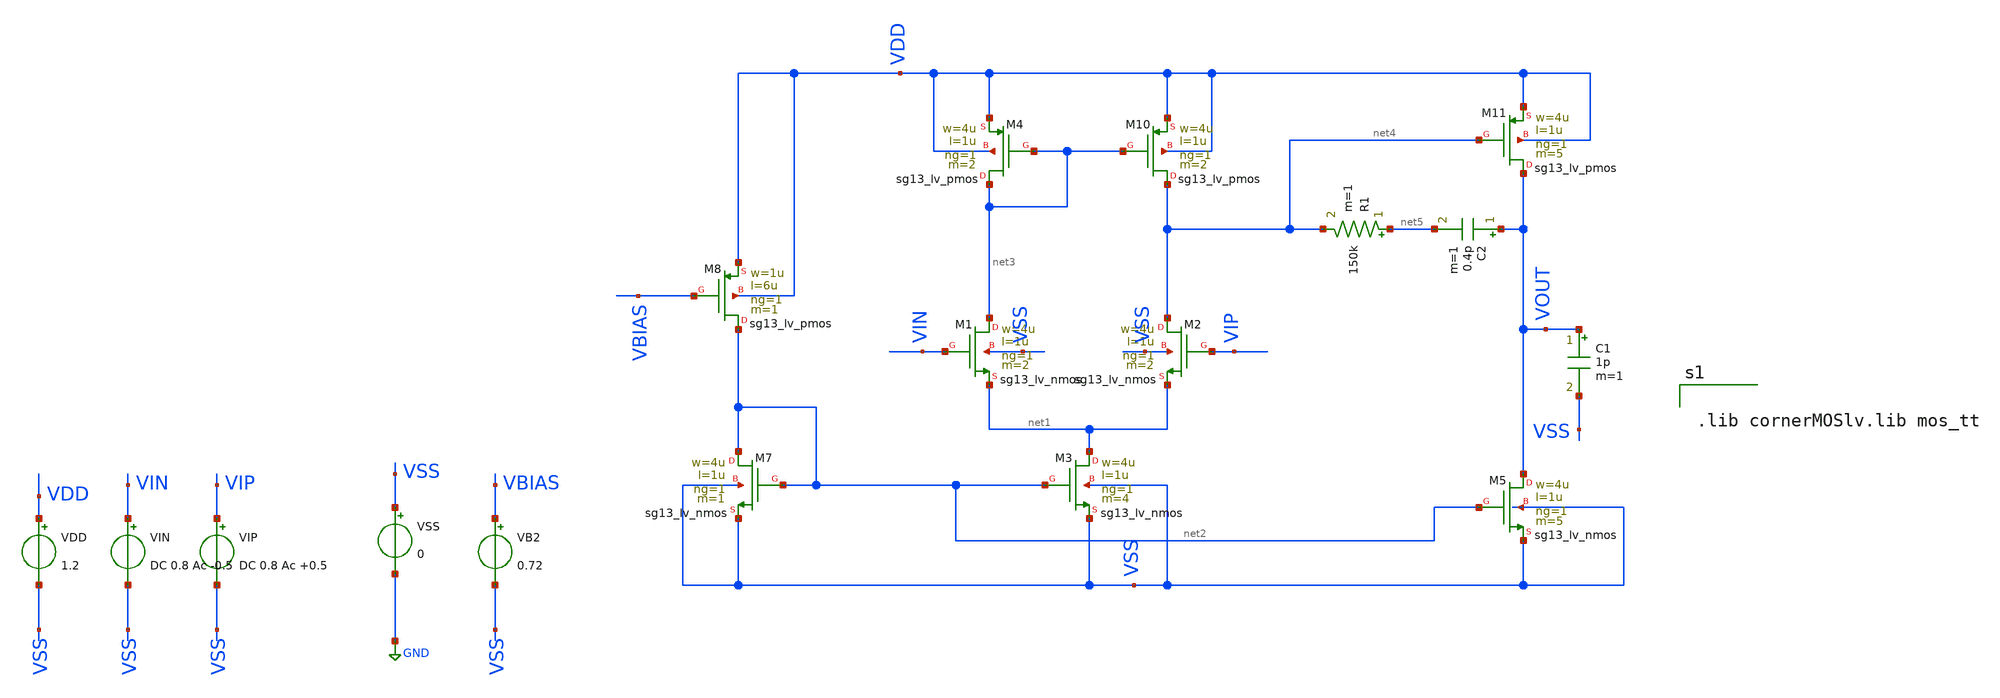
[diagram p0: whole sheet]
** sch_path: BTDay5-Ex/Ex1_6_Lecture5.sch
**.subckt Ex1_6_Lecture5
XM1 net3 VIN net1 VSS sg13_lv_nmos w=4u l=1u ng=1 m=2 mm_ok=1
XM2 net4 VIP net1 VSS sg13_lv_nmos w=4u l=1u ng=1 m=2 mm_ok=1
XM3 net1 net2 VSS VSS sg13_lv_nmos w=4u l=1u ng=1 m=4 mm_ok=1
VDD VDD VSS 1.2
VIN VIN VSS DC 0.8 Ac -0.5
VIP VIP VSS DC 0.8 Ac +0.5
VSS VSS GND 0
XM4 net3 net3 VDD VDD sg13_lv_pmos w=4u l=1u ng=1 m=2 mm_ok=1
XM7 net2 net2 VSS VSS sg13_lv_nmos w=4u l=1u ng=1 m=1 mm_ok=1
XM8 net2 VBIAS VDD VDD sg13_lv_pmos w=1u l=6u ng=1 m=1 mm_ok=1
XM10 net4 net3 VDD VDD sg13_lv_pmos w=4u l=1u ng=1 m=2 mm_ok=1
VB2 VBIAS VSS 0.72
XM5 VOUT net2 VSS VSS sg13_lv_nmos w=4u l=1u ng=1 m=5 mm_ok=1
XM11 VOUT net4 VDD VDD sg13_lv_pmos w=4u l=1u ng=1 m=5 mm_ok=1
C1 VOUT VSS 1p m=1
C2 VOUT net5 0.4p m=1
R1 net5 net4 150k m=1
**** begin user architecture code


.lib cornerMOSlv.lib mos_tt




.control

*==================================================
* 1. SAVE OPERATING-POINT PARAMETERS
*==================================================

save all

* NMOS
save @n.xm1.nsg13_lv_nmos[ids] @n.xm1.nsg13_lv_nmos[vgs] @n.xm1.nsg13_lv_nmos[vth]
+ @n.xm1.nsg13_lv_nmos[vds] @n.xm1.nsg13_lv_nmos[vdss] @n.xm1.nsg13_lv_nmos[gm] @n.xm1.nsg13_lv_nmos[gds]

save @n.xm2.nsg13_lv_nmos[ids] @n.xm2.nsg13_lv_nmos[vgs] @n.xm2.nsg13_lv_nmos[vth]
+ @n.xm2.nsg13_lv_nmos[vds] @n.xm2.nsg13_lv_nmos[vdss] @n.xm2.nsg13_lv_nmos[gm] @n.xm2.nsg13_lv_nmos[gds]

save @n.xm3.nsg13_lv_nmos[ids] @n.xm3.nsg13_lv_nmos[vgs] @n.xm3.nsg13_lv_nmos[vth]
+ @n.xm3.nsg13_lv_nmos[vds] @n.xm3.nsg13_lv_nmos[vdss] @n.xm3.nsg13_lv_nmos[gm] @n.xm3.nsg13_lv_nmos[gds]

save @n.xm5.nsg13_lv_nmos[ids] @n.xm5.nsg13_lv_nmos[vgs] @n.xm5.nsg13_lv_nmos[vth]
+ @n.xm5.nsg13_lv_nmos[vds] @n.xm5.nsg13_lv_nmos[vdss] @n.xm5.nsg13_lv_nmos[gm] @n.xm5.nsg13_lv_nmos[gds]

save @n.xm7.nsg13_lv_nmos[ids] @n.xm7.nsg13_lv_nmos[vgs] @n.xm7.nsg13_lv_nmos[vth]
+ @n.xm7.nsg13_lv_nmos[vds] @n.xm7.nsg13_lv_nmos[vdss] @n.xm7.nsg13_lv_nmos[gm] @n.xm7.nsg13_lv_nmos[gds]

* PMOS
save @n.xm4.nsg13_lv_pmos[ids] @n.xm4.nsg13_lv_pmos[vgs] @n.xm4.nsg13_lv_pmos[vth]
+ @n.xm4.nsg13_lv_pmos[vds] @n.xm4.nsg13_lv_pmos[vdss] @n.xm4.nsg13_lv_pmos[gm] @n.xm4.nsg13_lv_pmos[gds]

save @n.xm8.nsg13_lv_pmos[ids] @n.xm8.nsg13_lv_pmos[vgs] @n.xm8.nsg13_lv_pmos[vth]
+ @n.xm8.nsg13_lv_pmos[vds] @n.xm8.nsg13_lv_pmos[vdss] @n.xm8.nsg13_lv_pmos[gm] @n.xm8.nsg13_lv_pmos[gds]

save @n.xm10.nsg13_lv_pmos[ids] @n.xm10.nsg13_lv_pmos[vgs] @n.xm10.nsg13_lv_pmos[vth]
+ @n.xm10.nsg13_lv_pmos[vds] @n.xm10.nsg13_lv_pmos[vdss] @n.xm10.nsg13_lv_pmos[gm] @n.xm10.nsg13_lv_pmos[gds]

save @n.xm11.nsg13_lv_pmos[ids] @n.xm11.nsg13_lv_pmos[vgs] @n.xm11.nsg13_lv_pmos[vth]
+ @n.xm11.nsg13_lv_pmos[vds] @n.xm11.nsg13_lv_pmos[vdss] @n.xm11.nsg13_lv_pmos[gm] @n.xm11.nsg13_lv_pmos[gds]


*==================================================
* 2. DC OPERATING POINT
*==================================================

op

echo ================= M1 NMOS =================
print @n.xm1.nsg13_lv_nmos[vgs] @n.xm1.nsg13_lv_nmos[vth] @n.xm1.nsg13_lv_nmos[vds]
+ @n.xm1.nsg13_lv_nmos[vdss] @n.xm1.nsg13_lv_nmos[ids] @n.xm1.nsg13_lv_nmos[gm] @n.xm1.nsg13_lv_nmos[gds]

echo ================= M2 NMOS =================
print @n.xm2.nsg13_lv_nmos[vgs] @n.xm2.nsg13_lv_nmos[vth] @n.xm2.nsg13_lv_nmos[vds]
+ @n.xm2.nsg13_lv_nmos[vdss] @n.xm2.nsg13_lv_nmos[ids] @n.xm2.nsg13_lv_nmos[gm] @n.xm2.nsg13_lv_nmos[gds]

echo ================= M3 NMOS =================
print @n.xm3.nsg13_lv_nmos[vgs] @n.xm3.nsg13_lv_nmos[vth] @n.xm3.nsg13_lv_nmos[vds]
+ @n.xm3.nsg13_lv_nmos[vdss] @n.xm3.nsg13_lv_nmos[ids] @n.xm3.nsg13_lv_nmos[gm] @n.xm3.nsg13_lv_nmos[gds]

echo ================= M5 NMOS =================
print @n.xm5.nsg13_lv_nmos[vgs] @n.xm5.nsg13_lv_nmos[vth] @n.xm5.nsg13_lv_nmos[vds]
+ @n.xm5.nsg13_lv_nmos[vdss] @n.xm5.nsg13_lv_nmos[ids] @n.xm5.nsg13_lv_nmos[gm] @n.xm5.nsg13_lv_nmos[gds]

echo ================= M7 NMOS =================
print @n.xm7.nsg13_lv_nmos[vgs] @n.xm7.nsg13_lv_nmos[vth] @n.xm7.nsg13_lv_nmos[vds]
+ @n.xm7.nsg13_lv_nmos[vdss] @n.xm7.nsg13_lv_nmos[ids] @n.xm7.nsg13_lv_nmos[gm] @n.xm7.nsg13_lv_nmos[gds]

echo ================= M4 PMOS =================
print @n.xm4.nsg13_lv_pmos[vgs] @n.xm4.nsg13_lv_pmos[vth] @n.xm4.nsg13_lv_pmos[vds]
+ @n.xm4.nsg13_lv_pmos[vdss] @n.xm4.nsg13_lv_pmos[ids] @n.xm4.nsg13_lv_pmos[gm] @n.xm4.nsg13_lv_pmos[gds]

echo ================= M8 PMOS =================
print @n.xm8.nsg13_lv_pmos[vgs] @n.xm8.nsg13_lv_pmos[vth] @n.xm8.nsg13_lv_pmos[vds]
+ @n.xm8.nsg13_lv_pmos[vdss] @n.xm8.nsg13_lv_pmos[ids] @n.xm8.nsg13_lv_pmos[gm] @n.xm8.nsg13_lv_pmos[gds]

echo ================= M10 PMOS ================
print @n.xm10.nsg13_lv_pmos[vgs] @n.xm10.nsg13_lv_pmos[vth] @n.xm10.nsg13_lv_pmos[vds]
+ @n.xm10.nsg13_lv_pmos[vdss] @n.xm10.nsg13_lv_pmos[ids] @n.xm10.nsg13_lv_pmos[gm] @n.xm10.nsg13_lv_pmos[gds]

echo ================= M11 PMOS ================
print @n.xm11.nsg13_lv_pmos[vgs] @n.xm11.nsg13_lv_pmos[vth] @n.xm11.nsg13_lv_pmos[vds]
+ @n.xm11.nsg13_lv_pmos[vdss] @n.xm11.nsg13_lv_pmos[ids] @n.xm11.nsg13_lv_pmos[gm] @n.xm11.nsg13_lv_pmos[gds]
print v(vout)

write op_operating_point.raw


*==================================================
* 3. AC GAIN AND PHASE
*==================================================
ac dec 100 1 10G

let vid = v(vip)-v(vin)
let av = v(vout)/vid

let gain_db = db(av)
let phase_deg = cph(av)*180/pi


if phase_deg[0] > 90
    let phase_deg = phase_deg-360
end


meas ac f_ug when gain_db=0 fall=1
meas ac phase_at_ug find phase_deg when gain_db=0 fall=1
let phase_margin = 180+phase_at_ug

echo
echo ===== PHASE_MARGIN_RESULT =====
print f_ug phase_at_ug phase_margin


let line_0db = 0*frequency
let line_m180 = -180+0*frequency

plot gain_db phase_deg line_0db line_m180
xlog ylimit -360 80 title Gain

**** end user architecture code
**.ends
.GLOBAL GND
.end
